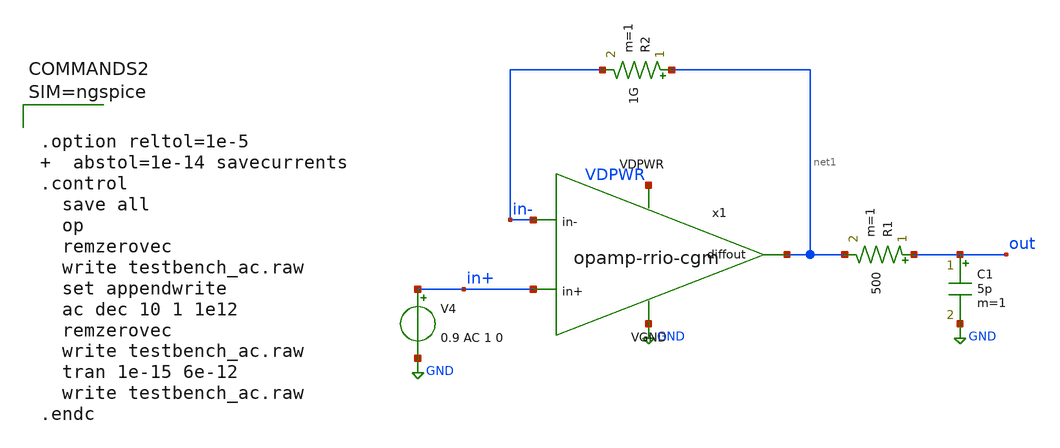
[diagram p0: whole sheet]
** sch_path: xschem/testbench_ac.sch
**.subckt testbench_ac
x1 VDPWR net1 in+ in- GND opamp-rrio-cgm
V4 in+ GND 0.9 AC 1 0
R2 net1 in- 1G m=1
C1 out GND 5p m=1
R1 out net1 500 m=1
**** begin user architecture code

** opencircuitdesign pdks install
.lib $::SKYWATER_MODELS/sky130.lib.spice tt





.option reltol=1e-5   abstol=1e-14 savecurrents
.control
  save all
  op
  remzerovec
  write testbench_ac.raw
  set appendwrite
  ac dec 10 1 1e12
  remzerovec
  write testbench_ac.raw
  tran 1e-15 6e-12
  write testbench_ac.raw
.endc



**** end user architecture code
**.ends

* expanding   symbol:  opamp-rrio-cgm.sym # of pins=5
** sym_path: xschem/opamp-rrio-cgm.sym
** sch_path: xschem/opamp-rrio-cgm.sch
.subckt opamp-rrio-cgm VDPWR diffout in+ in- VGND
*.ipin in-
*.ipin in+
*.opin diffout
*.ipin VDPWR
*.ipin VGND
XM1 net2 in- net3 VGND sky130_fd_pr__nfet_01v8_lvt L=0.36 W=50 nf=5 ad='int((nf+1)/2) * W/nf * 0.29'
+ as='int((nf+2)/2) * W/nf * 0.29' pd='2*int((nf+1)/2) * (W/nf + 0.29)' ps='2*int((nf+2)/2) * (W/nf + 0.29)'
+ nrd='0.29 / W' nrs='0.29 / W' sa=0 sb=0 sd=0 mult=1 m=1
XM3 drain in+ net3 VGND sky130_fd_pr__nfet_01v8_lvt L=0.36 W=50 nf=5 ad='int((nf+1)/2) * W/nf * 0.29'
+ as='int((nf+2)/2) * W/nf * 0.29' pd='2*int((nf+1)/2) * (W/nf + 0.29)' ps='2*int((nf+2)/2) * (W/nf + 0.29)'
+ nrd='0.29 / W' nrs='0.29 / W' sa=0 sb=0 sd=0 mult=1 m=1
XM7 drain bias net3 VGND sky130_fd_pr__nfet_01v8_lvt L=0.36 W=50 nf=5 ad='int((nf+1)/2) * W/nf * 0.29'
+ as='int((nf+2)/2) * W/nf * 0.29' pd='2*int((nf+1)/2) * (W/nf + 0.29)' ps='2*int((nf+2)/2) * (W/nf + 0.29)'
+ nrd='0.29 / W' nrs='0.29 / W' sa=0 sb=0 sd=0 mult=1 m=1
XM8 net2 bias net3 VGND sky130_fd_pr__nfet_01v8_lvt L=0.36 W=50 nf=5 ad='int((nf+1)/2) * W/nf * 0.29'
+ as='int((nf+2)/2) * W/nf * 0.29' pd='2*int((nf+1)/2) * (W/nf + 0.29)' ps='2*int((nf+2)/2) * (W/nf + 0.29)'
+ nrd='0.29 / W' nrs='0.29 / W' sa=0 sb=0 sd=0 mult=1 m=1
XM18 net6 bias3 net5 VGND sky130_fd_pr__nfet_01v8_lvt L=0.36 W=10 nf=1 ad='int((nf+1)/2) * W/nf * 0.29'
+ as='int((nf+2)/2) * W/nf * 0.29' pd='2*int((nf+1)/2) * (W/nf + 0.29)' ps='2*int((nf+2)/2) * (W/nf + 0.29)'
+ nrd='0.29 / W' nrs='0.29 / W' sa=0 sb=0 sd=0 mult=1 m=1
XM19 net12 bias3 net4 VGND sky130_fd_pr__nfet_01v8_lvt L=0.36 W=10 nf=1 ad='int((nf+1)/2) * W/nf * 0.29'
+ as='int((nf+2)/2) * W/nf * 0.29' pd='2*int((nf+1)/2) * (W/nf + 0.29)' ps='2*int((nf+2)/2) * (W/nf + 0.29)'
+ nrd='0.29 / W' nrs='0.29 / W' sa=0 sb=0 sd=0 mult=1 m=1
XM20 net5 bias4 VGND VGND sky130_fd_pr__nfet_01v8_lvt L=6 W=10 nf=1 ad='int((nf+1)/2) * W/nf * 0.29'
+ as='int((nf+2)/2) * W/nf * 0.29' pd='2*int((nf+1)/2) * (W/nf + 0.29)' ps='2*int((nf+2)/2) * (W/nf + 0.29)'
+ nrd='0.29 / W' nrs='0.29 / W' sa=0 sb=0 sd=0 mult=1 m=1
XM21 net4 bias4 VGND VGND sky130_fd_pr__nfet_01v8_lvt L=6 W=10 nf=1 ad='int((nf+1)/2) * W/nf * 0.29'
+ as='int((nf+2)/2) * W/nf * 0.29' pd='2*int((nf+1)/2) * (W/nf + 0.29)' ps='2*int((nf+2)/2) * (W/nf + 0.29)'
+ nrd='0.29 / W' nrs='0.29 / W' sa=0 sb=0 sd=0 mult=1 m=1
XM22 net3 bias4 VGND VGND sky130_fd_pr__nfet_01v8_lvt L=6 W=10 nf=1 ad='int((nf+1)/2) * W/nf * 0.29'
+ as='int((nf+2)/2) * W/nf * 0.29' pd='2*int((nf+1)/2) * (W/nf + 0.29)' ps='2*int((nf+2)/2) * (W/nf + 0.29)'
+ nrd='0.29 / W' nrs='0.29 / W' sa=0 sb=0 sd=0 mult=1 m=1
XM25 net8 net8 net11 VGND sky130_fd_pr__nfet_01v8_lvt L=0.18 W=30 nf=1 ad='int((nf+1)/2) * W/nf * 0.29'
+ as='int((nf+2)/2) * W/nf * 0.29' pd='2*int((nf+1)/2) * (W/nf + 0.29)' ps='2*int((nf+2)/2) * (W/nf + 0.29)'
+ nrd='0.29 / W' nrs='0.29 / W' sa=0 sb=0 sd=0 mult=1 m=1
XM26 net10 net8 net12 VGND sky130_fd_pr__nfet_01v8_lvt L=0.18 W=30 nf=1 ad='int((nf+1)/2) * W/nf * 0.29'
+ as='int((nf+2)/2) * W/nf * 0.29' pd='2*int((nf+1)/2) * (W/nf + 0.29)' ps='2*int((nf+2)/2) * (W/nf + 0.29)'
+ nrd='0.29 / W' nrs='0.29 / W' sa=0 sb=0 sd=0 mult=1 m=1
XM30 net11 net11 VGND VGND sky130_fd_pr__nfet_01v8_lvt L=0.18 W=5 nf=1 ad='int((nf+1)/2) * W/nf * 0.29'
+ as='int((nf+2)/2) * W/nf * 0.29' pd='2*int((nf+1)/2) * (W/nf + 0.29)' ps='2*int((nf+2)/2) * (W/nf + 0.29)'
+ nrd='0.29 / W' nrs='0.29 / W' sa=0 sb=0 sd=0 mult=1 m=1
XM31 net9 bias4 VGND VGND sky130_fd_pr__nfet_01v8_lvt L=6 W=2.5 nf=1 ad='int((nf+1)/2) * W/nf * 0.29'
+ as='int((nf+2)/2) * W/nf * 0.29' pd='2*int((nf+1)/2) * (W/nf + 0.29)' ps='2*int((nf+2)/2) * (W/nf + 0.29)'
+ nrd='0.29 / W' nrs='0.29 / W' sa=0 sb=0 sd=0 mult=1 m=1
XM32 diffout net12 VGND VGND sky130_fd_pr__nfet_01v8_lvt L=0.18 W=60 nf=17 ad='int((nf+1)/2) * W/nf * 0.29'
+ as='int((nf+2)/2) * W/nf * 0.29' pd='2*int((nf+1)/2) * (W/nf + 0.29)' ps='2*int((nf+2)/2) * (W/nf + 0.29)'
+ nrd='0.29 / W' nrs='0.29 / W' sa=0 sb=0 sd=0 mult=2 m=2
XM33 bias4 bias4 VGND VGND sky130_fd_pr__nfet_01v8_lvt L=6 W=10 nf=1 ad='int((nf+1)/2) * W/nf * 0.29'
+ as='int((nf+2)/2) * W/nf * 0.29' pd='2*int((nf+1)/2) * (W/nf + 0.29)' ps='2*int((nf+2)/2) * (W/nf + 0.29)'
+ nrd='0.29 / W' nrs='0.29 / W' sa=0 sb=0 sd=0 mult=1 m=1
XC1 diffout drain sky130_fd_pr__cap_mim_m3_1 W=15 L=15 MF=1 m=1
XC2 diffout net4 sky130_fd_pr__cap_mim_m3_1 W=24 L=24 MF=1 m=1
XM5 bias4 bias4 bias1 VDPWR sky130_fd_pr__pfet_01v8_lvt L=0.35 W=1 nf=1 ad='int((nf+1)/2) * W/nf * 0.29'
+ as='int((nf+2)/2) * W/nf * 0.29' pd='2*int((nf+1)/2) * (W/nf + 0.29)' ps='2*int((nf+2)/2) * (W/nf + 0.29)'
+ nrd='0.29 / W' nrs='0.29 / W' sa=0 sb=0 sd=0 mult=1 m=1
XM6 bias1 bias1 VDPWR VDPWR sky130_fd_pr__pfet_01v8_lvt L=6 W=33 nf=1 ad='int((nf+1)/2) * W/nf * 0.29'
+ as='int((nf+2)/2) * W/nf * 0.29' pd='2*int((nf+1)/2) * (W/nf + 0.29)' ps='2*int((nf+2)/2) * (W/nf + 0.29)'
+ nrd='0.29 / W' nrs='0.29 / W' sa=0 sb=0 sd=0 mult=1 m=1
XM13 net1 bias1 VDPWR VDPWR sky130_fd_pr__pfet_01v8_lvt L=6 W=33 nf=2 ad='int((nf+1)/2) * W/nf * 0.29'
+ as='int((nf+2)/2) * W/nf * 0.29' pd='2*int((nf+1)/2) * (W/nf + 0.29)' ps='2*int((nf+2)/2) * (W/nf + 0.29)'
+ nrd='0.29 / W' nrs='0.29 / W' sa=0 sb=0 sd=0 mult=1 m=1
XM14 net2 net6 VDPWR VDPWR sky130_fd_pr__pfet_01v8_lvt L=6 W=33 nf=1 ad='int((nf+1)/2) * W/nf * 0.29'
+ as='int((nf+2)/2) * W/nf * 0.29' pd='2*int((nf+1)/2) * (W/nf + 0.29)' ps='2*int((nf+2)/2) * (W/nf + 0.29)'
+ nrd='0.29 / W' nrs='0.29 / W' sa=0 sb=0 sd=0 mult=1 m=1
XM15 drain net6 VDPWR VDPWR sky130_fd_pr__pfet_01v8_lvt L=6 W=33 nf=1 ad='int((nf+1)/2) * W/nf * 0.29'
+ as='int((nf+2)/2) * W/nf * 0.29' pd='2*int((nf+1)/2) * (W/nf + 0.29)' ps='2*int((nf+2)/2) * (W/nf + 0.29)'
+ nrd='0.29 / W' nrs='0.29 / W' sa=0 sb=0 sd=0 mult=1 m=1
XM16 net10 bias2 drain VDPWR sky130_fd_pr__pfet_01v8_lvt L=0.36 W=33 nf=1 ad='int((nf+1)/2) * W/nf * 0.29'
+ as='int((nf+2)/2) * W/nf * 0.29' pd='2*int((nf+1)/2) * (W/nf + 0.29)' ps='2*int((nf+2)/2) * (W/nf + 0.29)'
+ nrd='0.29 / W' nrs='0.29 / W' sa=0 sb=0 sd=0 mult=1 m=1
XM23 net8 bias1 VDPWR VDPWR sky130_fd_pr__pfet_01v8_lvt L=6 W=8.25 nf=1 ad='int((nf+1)/2) * W/nf * 0.29'
+ as='int((nf+2)/2) * W/nf * 0.29' pd='2*int((nf+1)/2) * (W/nf + 0.29)' ps='2*int((nf+2)/2) * (W/nf + 0.29)'
+ nrd='0.29 / W' nrs='0.29 / W' sa=0 sb=0 sd=0 mult=1 m=1
XM24 net6 bias2 net2 VDPWR sky130_fd_pr__pfet_01v8_lvt L=0.36 W=33 nf=1 ad='int((nf+1)/2) * W/nf * 0.29'
+ as='int((nf+2)/2) * W/nf * 0.29' pd='2*int((nf+1)/2) * (W/nf + 0.29)' ps='2*int((nf+2)/2) * (W/nf + 0.29)'
+ nrd='0.29 / W' nrs='0.29 / W' sa=0 sb=0 sd=0 mult=1 m=1
XM28 net7 net7 VDPWR VDPWR sky130_fd_pr__pfet_01v8_lvt L=0.35 W=16.5 nf=5 ad='int((nf+1)/2) * W/nf * 0.29'
+ as='int((nf+2)/2) * W/nf * 0.29' pd='2*int((nf+1)/2) * (W/nf + 0.29)' ps='2*int((nf+2)/2) * (W/nf + 0.29)'
+ nrd='0.29 / W' nrs='0.29 / W' sa=0 sb=0 sd=0 mult=1 m=1
XM29 diffout net10 VDPWR VDPWR sky130_fd_pr__pfet_01v8_lvt L=0.35 W=198 nf=11 ad='int((nf+1)/2) * W/nf * 0.29'
+ as='int((nf+2)/2) * W/nf * 0.29' pd='2*int((nf+1)/2) * (W/nf + 0.29)' ps='2*int((nf+2)/2) * (W/nf + 0.29)'
+ nrd='0.29 / W' nrs='0.29 / W' sa=0 sb=0 sd=0 mult=2 m=2
XM34 net9 net9 net7 VDPWR sky130_fd_pr__pfet_01v8_lvt L=0.35 W=99 nf=1 ad='int((nf+1)/2) * W/nf * 0.29'
+ as='int((nf+2)/2) * W/nf * 0.29' pd='2*int((nf+1)/2) * (W/nf + 0.29)' ps='2*int((nf+2)/2) * (W/nf + 0.29)'
+ nrd='0.29 / W' nrs='0.29 / W' sa=0 sb=0 sd=0 mult=1 m=1
XM35 net12 net9 net10 VDPWR sky130_fd_pr__pfet_01v8_lvt L=0.35 W=99 nf=1 ad='int((nf+1)/2) * W/nf * 0.29'
+ as='int((nf+2)/2) * W/nf * 0.29' pd='2*int((nf+1)/2) * (W/nf + 0.29)' ps='2*int((nf+2)/2) * (W/nf + 0.29)'
+ nrd='0.29 / W' nrs='0.29 / W' sa=0 sb=0 sd=0 mult=1 m=1
XM2 net4 bias net1 VDPWR sky130_fd_pr__pfet_01v8_lvt L=0.36 W=165 nf=10 ad='int((nf+1)/2) * W/nf * 0.29'
+ as='int((nf+2)/2) * W/nf * 0.29' pd='2*int((nf+1)/2) * (W/nf + 0.29)' ps='2*int((nf+2)/2) * (W/nf + 0.29)'
+ nrd='0.29 / W' nrs='0.29 / W' sa=0 sb=0 sd=0 mult=2 m=2
XM4 net5 bias net1 VDPWR sky130_fd_pr__pfet_01v8_lvt L=0.36 W=165 nf=10 ad='int((nf+1)/2) * W/nf * 0.29'
+ as='int((nf+2)/2) * W/nf * 0.29' pd='2*int((nf+1)/2) * (W/nf + 0.29)' ps='2*int((nf+2)/2) * (W/nf + 0.29)'
+ nrd='0.29 / W' nrs='0.29 / W' sa=0 sb=0 sd=0 mult=2 m=2
XM9 net5 in- net1 VDPWR sky130_fd_pr__pfet_01v8_lvt L=0.36 W=165 nf=10 ad='int((nf+1)/2) * W/nf * 0.29'
+ as='int((nf+2)/2) * W/nf * 0.29' pd='2*int((nf+1)/2) * (W/nf + 0.29)' ps='2*int((nf+2)/2) * (W/nf + 0.29)'
+ nrd='0.29 / W' nrs='0.29 / W' sa=0 sb=0 sd=0 mult=2 m=2
XM10 net4 in+ net1 VDPWR sky130_fd_pr__pfet_01v8_lvt L=0.36 W=165 nf=10 ad='int((nf+1)/2) * W/nf * 0.29'
+ as='int((nf+2)/2) * W/nf * 0.29' pd='2*int((nf+1)/2) * (W/nf + 0.29)' ps='2*int((nf+2)/2) * (W/nf + 0.29)'
+ nrd='0.29 / W' nrs='0.29 / W' sa=0 sb=0 sd=0 mult=2 m=2
XM11 net13 net13 VDPWR VDPWR sky130_fd_pr__pfet_01v8_lvt L=0.36 W=33 nf=1 ad='int((nf+1)/2) * W/nf * 0.29'
+ as='int((nf+2)/2) * W/nf * 0.29' pd='2*int((nf+1)/2) * (W/nf + 0.29)' ps='2*int((nf+2)/2) * (W/nf + 0.29)'
+ nrd='0.29 / W' nrs='0.29 / W' sa=0 sb=0 sd=0 mult=1 m=1
XM12 bias2 bias2 net13 VDPWR sky130_fd_pr__pfet_01v8_lvt L=0.36 W=33 nf=1 ad='int((nf+1)/2) * W/nf * 0.29'
+ as='int((nf+2)/2) * W/nf * 0.29' pd='2*int((nf+1)/2) * (W/nf + 0.29)' ps='2*int((nf+2)/2) * (W/nf + 0.29)'
+ nrd='0.29 / W' nrs='0.29 / W' sa=0 sb=0 sd=0 mult=1 m=1
XM17 bias3 bias3 VGND VGND sky130_fd_pr__nfet_01v8_lvt L=0.36 W=10 nf=1 ad='int((nf+1)/2) * W/nf * 0.29'
+ as='int((nf+2)/2) * W/nf * 0.29' pd='2*int((nf+1)/2) * (W/nf + 0.29)' ps='2*int((nf+2)/2) * (W/nf + 0.29)'
+ nrd='0.29 / W' nrs='0.29 / W' sa=0 sb=0 sd=0 mult=1 m=1
XM27 bias2 bias2 bias3 VGND sky130_fd_pr__nfet_01v8_lvt L=0.36 W=10 nf=1 ad='int((nf+1)/2) * W/nf * 0.29'
+ as='int((nf+2)/2) * W/nf * 0.29' pd='2*int((nf+1)/2) * (W/nf + 0.29)' ps='2*int((nf+2)/2) * (W/nf + 0.29)'
+ nrd='0.29 / W' nrs='0.29 / W' sa=0 sb=0 sd=0 mult=1 m=1
XM36 net14 net14 VDPWR VDPWR sky130_fd_pr__pfet_01v8_lvt L=0.36 W=5 nf=1 ad='int((nf+1)/2) * W/nf * 0.29'
+ as='int((nf+2)/2) * W/nf * 0.29' pd='2*int((nf+1)/2) * (W/nf + 0.29)' ps='2*int((nf+2)/2) * (W/nf + 0.29)'
+ nrd='0.29 / W' nrs='0.29 / W' sa=0 sb=0 sd=0 mult=1 m=1
XM37 bias bias net14 VDPWR sky130_fd_pr__pfet_01v8_lvt L=0.36 W=5 nf=1 ad='int((nf+1)/2) * W/nf * 0.29'
+ as='int((nf+2)/2) * W/nf * 0.29' pd='2*int((nf+1)/2) * (W/nf + 0.29)' ps='2*int((nf+2)/2) * (W/nf + 0.29)'
+ nrd='0.29 / W' nrs='0.29 / W' sa=0 sb=0 sd=0 mult=1 m=1
XM38 bias bias VGND VGND sky130_fd_pr__nfet_01v8_lvt L=0.36 W=30 nf=1 ad='int((nf+1)/2) * W/nf * 0.29'
+ as='int((nf+2)/2) * W/nf * 0.29' pd='2*int((nf+1)/2) * (W/nf + 0.29)' ps='2*int((nf+2)/2) * (W/nf + 0.29)'
+ nrd='0.29 / W' nrs='0.29 / W' sa=0 sb=0 sd=0 mult=1 m=1
.ends

.GLOBAL GND
.end
